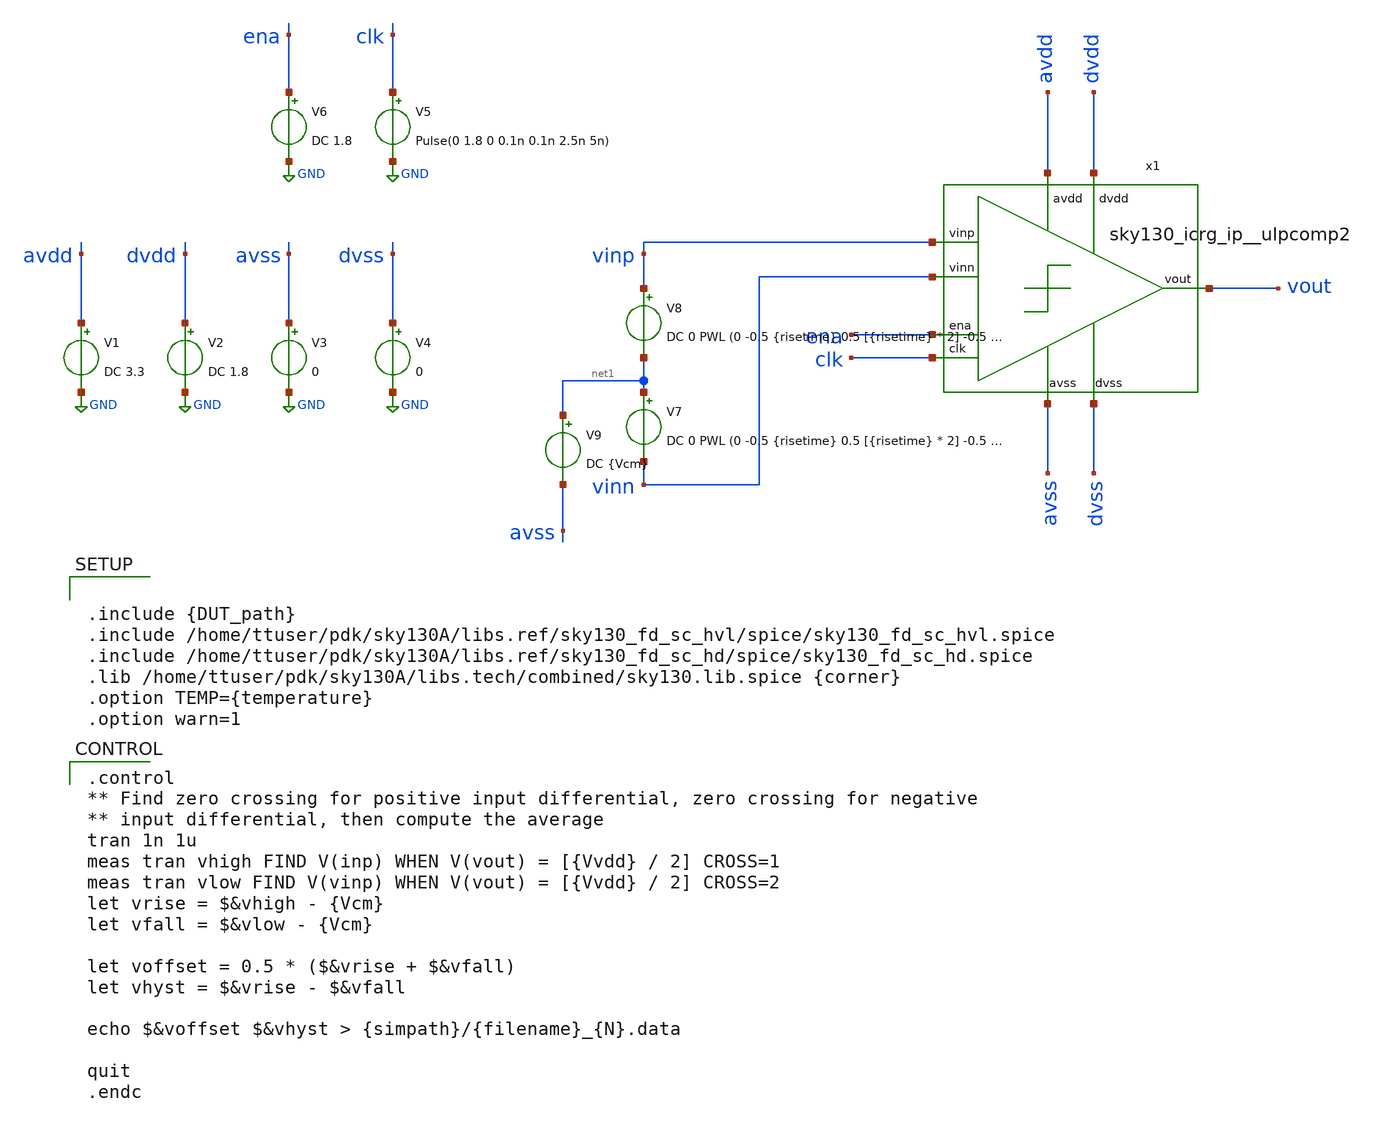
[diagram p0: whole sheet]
** sch_path: cace/inputoffset.sch
**.subckt inputoffset
x1 dvdd avdd ena vout vinn vinp clk dvss avss sky130_icrg_ip__ulpcomp2
V1 avdd GND DC 3.3
V2 dvdd GND DC 1.8
V3 avss GND 0
V4 dvss GND 0
V5 clk GND Pulse(0 1.8 0 0.1n 0.1n 2.5n 5n)
V6 ena GND DC 1.8
V7 net1 vinn DC 0 PWL (0 -0.5 {risetime} 0.5 [{risetime} * 2] -0.5 [{risetime} * 3] 0.5 [{risetime} *
+ 4] -0.5 )
V8 vinp net1 DC 0 PWL (0 -0.5 {risetime} 0.5 [{risetime} * 2] -0.5 [{risetime} * 3] 0.5 [{risetime} *
+ 4] -0.5 )
V9 net1 avss DC {Vcm}
**** begin user architecture code


.include {DUT_path}
.include /home/ttuser/pdk/sky130A/libs.ref/sky130_fd_sc_hvl/spice/sky130_fd_sc_hvl.spice
.include /home/ttuser/pdk/sky130A/libs.ref/sky130_fd_sc_hd/spice/sky130_fd_sc_hd.spice
.lib /home/ttuser/pdk/sky130A/libs.tech/combined/sky130.lib.spice {corner}
.option TEMP={temperature}
.option warn=1


.control
** Find zero crossing for positive input differential, zero crossing for negative
** input differential, then compute the average
tran 1n 1u
meas tran vhigh FIND V(inp) WHEN V(vout) = [{Vvdd} / 2] CROSS=1
meas tran vlow FIND V(vinp) WHEN V(vout) = [{Vvdd} / 2] CROSS=2
let vrise = $&vhigh - {Vcm}
let vfall = $&vlow - {Vcm}

let voffset = 0.5 * ($&vrise + $&vfall)
let vhyst = $&vrise - $&vfall

echo $&voffset $&vhyst > {simpath}/{filename}_{N}.data

quit
.endc


**** end user architecture code
**.ends
.GLOBAL GND
.end
